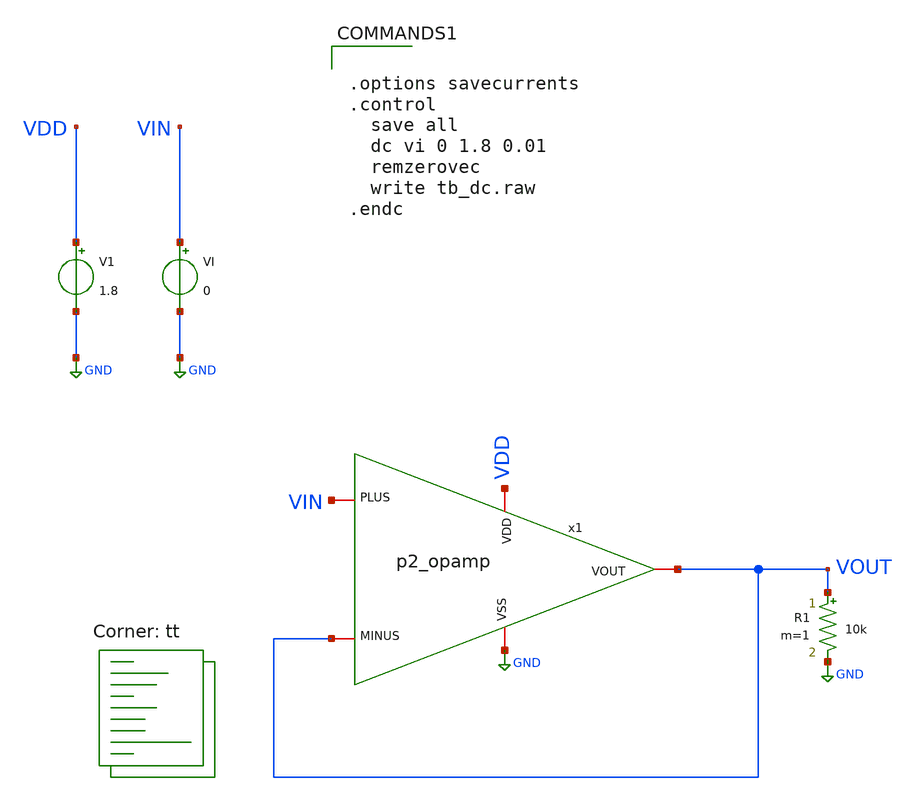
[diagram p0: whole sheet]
** sch_path: xschem/tb_dc.sch
**.subckt tb_dc
x1 VDD VOUT VIN VOUT GND p2_opamp
V1 VDD GND 1.8
R1 VOUT GND 10k m=1
VI VIN GND 0
**** begin user architecture code
.lib $::SKYWATER_MODELS/sky130.lib.spice tt


.options savecurrents
.control
  save all
  dc vi 0 1.8 0.01
  remzerovec
  write tb_dc.raw
.endc


**** end user architecture code
**.ends

* expanding   symbol:  p2_opamp.sym # of pins=5
** sym_path: xschem/p2_opamp.sym
** sch_path: xschem/p2_opamp.sch
.subckt p2_opamp VDD MINUS PLUS VOUT VSS
*.iopin VDD
*.iopin VSS
*.iopin PLUS
*.iopin MINUS
*.iopin VOUT
XM2 net2 MINUS net1 VSS sky130_fd_pr__nfet_01v8 L=0.15 W=16 nf=1 ad='int((nf+1)/2) * W/nf * 0.29' as='int((nf+2)/2) * W/nf * 0.29'
+ pd='2*int((nf+1)/2) * (W/nf + 0.29)' ps='2*int((nf+2)/2) * (W/nf + 0.29)' nrd='0.29 / W' nrs='0.29 / W'
+ sa=0 sb=0 sd=0 mult=1 m=1
XM1 net4 PLUS net1 VSS sky130_fd_pr__nfet_01v8 L=0.15 W=16 nf=1 ad='int((nf+1)/2) * W/nf * 0.29' as='int((nf+2)/2) * W/nf * 0.29'
+ pd='2*int((nf+1)/2) * (W/nf + 0.29)' ps='2*int((nf+2)/2) * (W/nf + 0.29)' nrd='0.29 / W' nrs='0.29 / W'
+ sa=0 sb=0 sd=0 mult=1 m=1
XM3 net1 net3 VSS VSS sky130_fd_pr__nfet_01v8 L=0.15 W=4 nf=1 ad='int((nf+1)/2) * W/nf * 0.29' as='int((nf+2)/2) * W/nf * 0.29'
+ pd='2*int((nf+1)/2) * (W/nf + 0.29)' ps='2*int((nf+2)/2) * (W/nf + 0.29)' nrd='0.29 / W' nrs='0.29 / W'
+ sa=0 sb=0 sd=0 mult=1 m=1
XM4 net2 net2 VDD VDD sky130_fd_pr__pfet_01v8 L=0.15 W=32 nf=1 ad='int((nf+1)/2) * W/nf * 0.29' as='int((nf+2)/2) * W/nf * 0.29'
+ pd='2*int((nf+1)/2) * (W/nf + 0.29)' ps='2*int((nf+2)/2) * (W/nf + 0.29)' nrd='0.29 / W' nrs='0.29 / W'
+ sa=0 sb=0 sd=0 mult=1 m=1
XM5 net4 net2 VDD VDD sky130_fd_pr__pfet_01v8 L=0.15 W=32 nf=1 ad='int((nf+1)/2) * W/nf * 0.29' as='int((nf+2)/2) * W/nf * 0.29'
+ pd='2*int((nf+1)/2) * (W/nf + 0.29)' ps='2*int((nf+2)/2) * (W/nf + 0.29)' nrd='0.29 / W' nrs='0.29 / W'
+ sa=0 sb=0 sd=0 mult=1 m=1
XM6 net3 net3 VSS VSS sky130_fd_pr__nfet_01v8 L=0.15 W=1 nf=1 ad='int((nf+1)/2) * W/nf * 0.29' as='int((nf+2)/2) * W/nf * 0.29'
+ pd='2*int((nf+1)/2) * (W/nf + 0.29)' ps='2*int((nf+2)/2) * (W/nf + 0.29)' nrd='0.29 / W' nrs='0.29 / W'
+ sa=0 sb=0 sd=0 mult=1 m=1
XM7 VOUT net3 VSS VSS sky130_fd_pr__nfet_01v8 L=0.15 W=8 nf=1 ad='int((nf+1)/2) * W/nf * 0.29' as='int((nf+2)/2) * W/nf * 0.29'
+ pd='2*int((nf+1)/2) * (W/nf + 0.29)' ps='2*int((nf+2)/2) * (W/nf + 0.29)' nrd='0.29 / W' nrs='0.29 / W'
+ sa=0 sb=0 sd=0 mult=1 m=1
XM8 VOUT net4 VDD VDD sky130_fd_pr__pfet_01v8 L=0.15 W=40 nf=1 ad='int((nf+1)/2) * W/nf * 0.29' as='int((nf+2)/2) * W/nf * 0.29'
+ pd='2*int((nf+1)/2) * (W/nf + 0.29)' ps='2*int((nf+2)/2) * (W/nf + 0.29)' nrd='0.29 / W' nrs='0.29 / W'
+ sa=0 sb=0 sd=0 mult=1 m=1
XC1 VOUT net4 sky130_fd_pr__cap_mim_m3_2 W=1 L=1 MF=1 m=1
XR1 net3 VDD VSS sky130_fd_pr__res_xhigh_po_5p73 L=150 mult=1 m=1
.ends

.GLOBAL GND
.end
